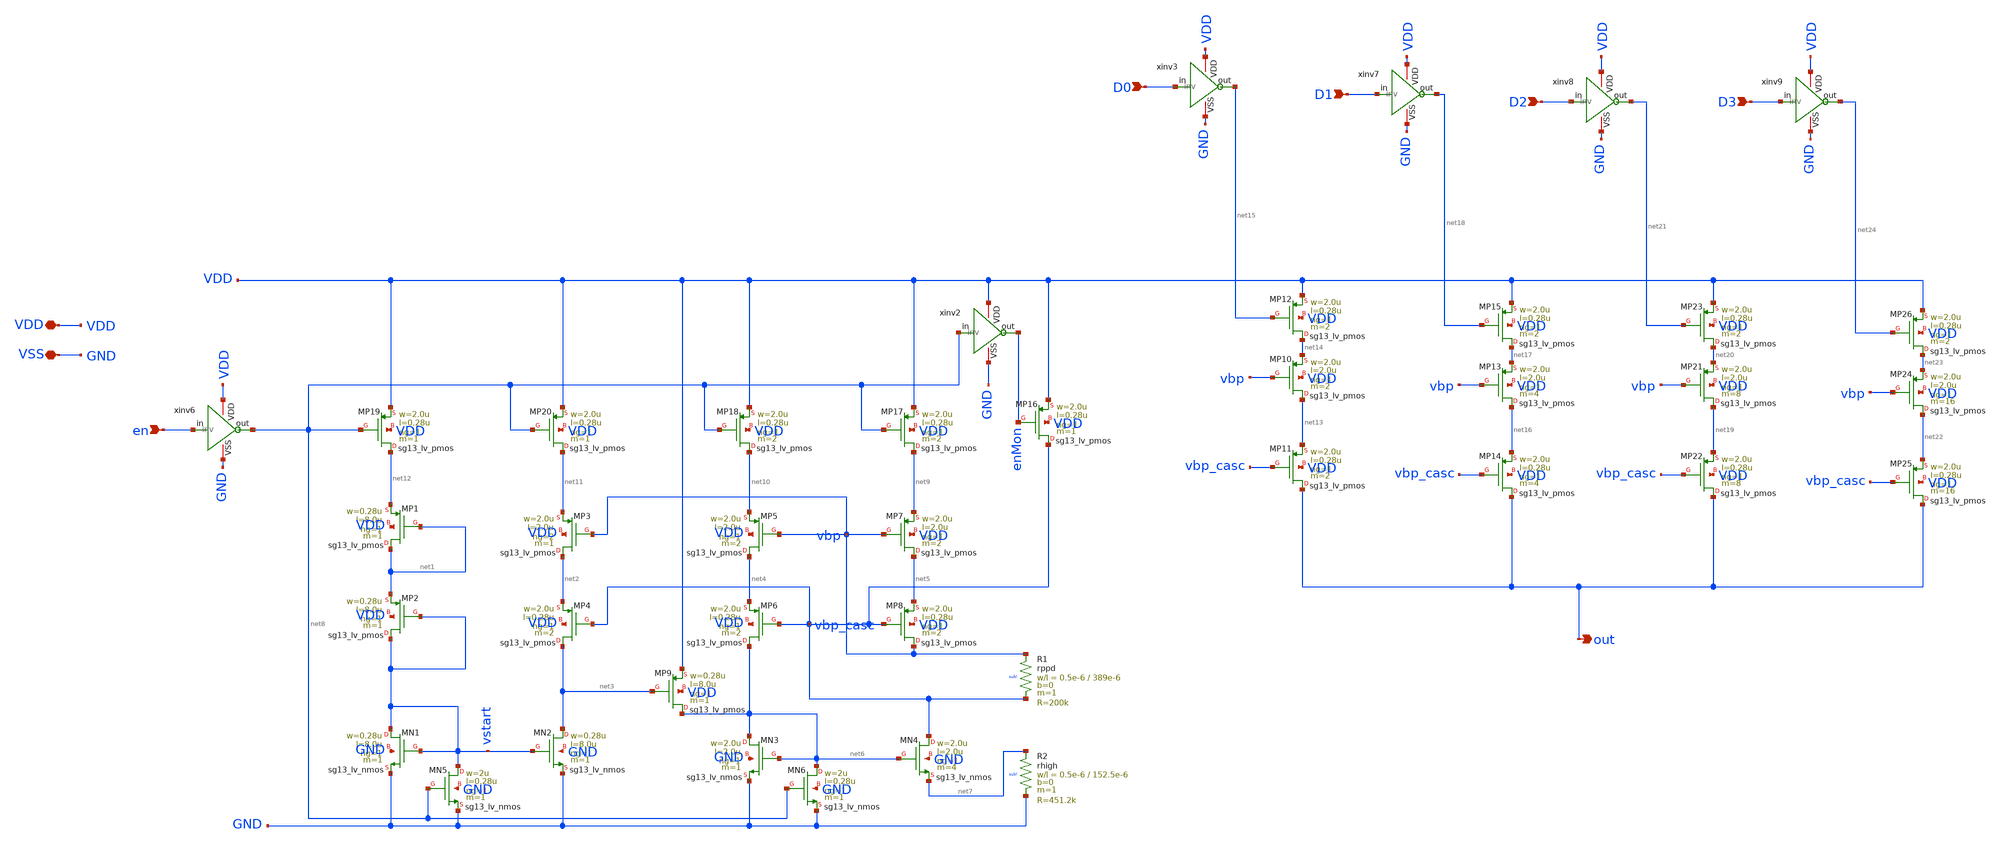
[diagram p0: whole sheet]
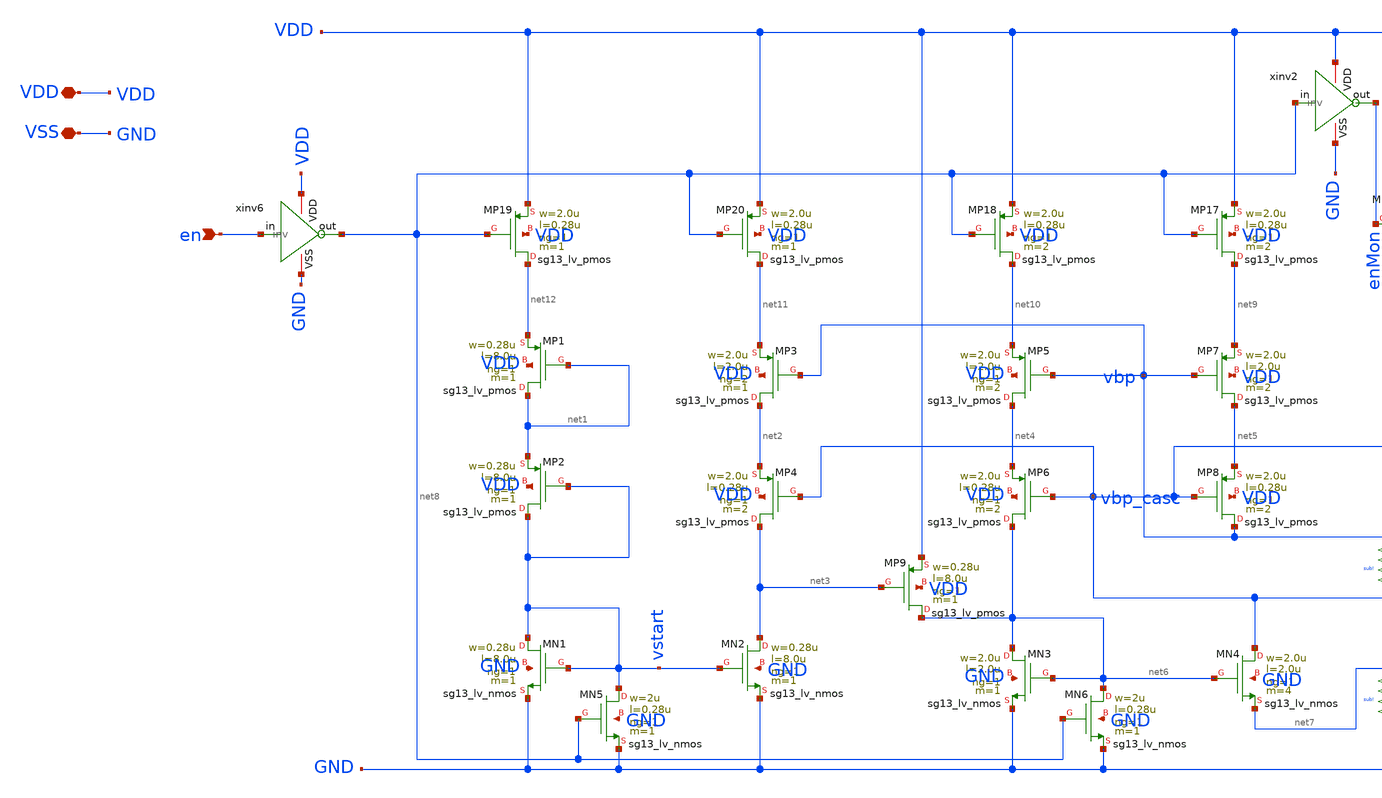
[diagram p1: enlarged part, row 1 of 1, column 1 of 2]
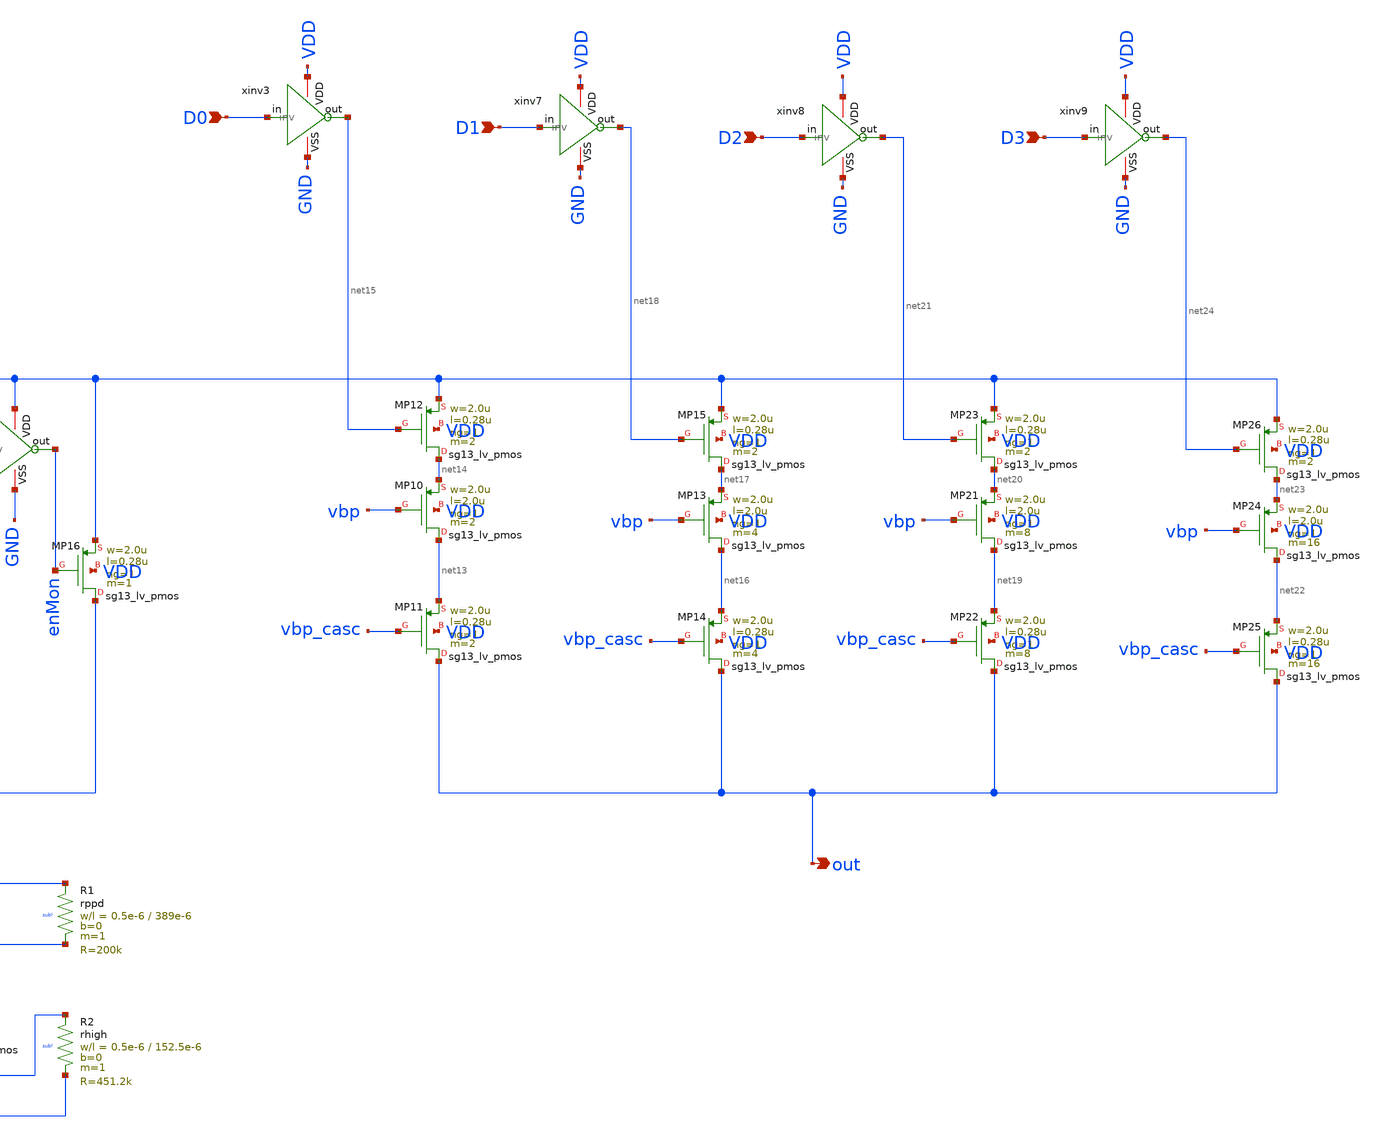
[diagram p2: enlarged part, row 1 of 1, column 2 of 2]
** sch_path: blocks/composite/dpi_adexp_neuron/design_data/xschem/trimmer.sch
**.subckt trimmer en D0 D1 D2 D3 out VDD VSS
*.ipin en
*.ipin D0
*.ipin D1
*.ipin D2
*.ipin D3
*.opin out
*.iopin VDD
*.iopin VSS
XMP1 net1 net1 net12 VDD sg13_lv_pmos w=0.28u l=8.0u ng=1 m=1 mm_ok=1
XMP2 vstart vstart net1 VDD sg13_lv_pmos w=0.28u l=8.0u ng=1 m=1 mm_ok=1
XMN2 net3 vstart GND GND sg13_lv_nmos w=0.28u l=8.0u ng=1 m=1 mm_ok=1
XMN1 vstart vstart GND GND sg13_lv_nmos w=0.28u l=8.0u ng=1 m=1 mm_ok=1
XMP3 net2 vbp net11 VDD sg13_lv_pmos w=2.0u l=2.0u ng=2 m=1 mm_ok=1
XMP4 net3 vbp_casc net2 VDD sg13_lv_pmos w=2.0u l=0.28u ng=1 m=2 mm_ok=1
XMP5 net4 vbp net10 VDD sg13_lv_pmos w=2.0u l=2.0u ng=1 m=2 mm_ok=1
XMP6 net6 vbp_casc net4 VDD sg13_lv_pmos w=2.0u l=0.28u ng=1 m=2 mm_ok=1
XMP7 net5 vbp net9 VDD sg13_lv_pmos w=2.0u l=2.0u ng=1 m=2 mm_ok=1
XMP8 vbp vbp_casc net5 VDD sg13_lv_pmos w=2.0u l=0.28u ng=1 m=2 mm_ok=1
XMP9 net6 net3 VDD VDD sg13_lv_pmos w=0.28u l=8.0u ng=1 m=1 mm_ok=1
XMN3 net6 net6 GND GND sg13_lv_nmos w=2.0u l=2.0u ng=1 m=1 mm_ok=1
XMN4 vbp_casc net6 net7 GND sg13_lv_nmos w=2.0u l=2.0u ng=1 m=4 mm_ok=1
XR1 vbp vbp_casc sub! rppd w=0.5e-6 l=389e-6 m=1 b=0 mm_ok=1
XR2 net7 GND sub! rhigh w=0.5e-6 l=152.5e-6 m=1 b=0 mm_ok=1
XMP10 net13 vbp net14 VDD sg13_lv_pmos w=2.0u l=2.0u ng=1 m=2 mm_ok=1
XMP11 out vbp_casc net13 VDD sg13_lv_pmos w=2.0u l=0.28u ng=1 m=2 mm_ok=1
XMP16 vbp_casc enMon VDD VDD sg13_lv_pmos w=2.0u l=0.28u ng=1 m=1 mm_ok=1
XMP17 net9 net8 VDD VDD sg13_lv_pmos w=2.0u l=0.28u ng=1 m=2 mm_ok=1
XMP18 net10 net8 VDD VDD sg13_lv_pmos w=2.0u l=0.28u ng=1 m=2 mm_ok=1
XMP19 net12 net8 VDD VDD sg13_lv_pmos w=2.0u l=0.28u ng=1 m=1 mm_ok=1
XMP20 net11 net8 VDD VDD sg13_lv_pmos w=2.0u l=0.28u ng=1 m=1 mm_ok=1
XMN5 vstart net8 GND GND sg13_lv_nmos w=2u l=0.28u ng=1 m=1 mm_ok=1
XMN6 net6 net8 GND GND sg13_lv_nmos w=2u l=0.28u ng=1 m=1 mm_ok=1
xinv2 VDD net8 enMon GND inv
XMP12 net14 net15 VDD VDD sg13_lv_pmos w=2.0u l=0.28u ng=1 m=2 mm_ok=1
XMP13 net16 vbp net17 VDD sg13_lv_pmos w=2.0u l=2.0u ng=1 m=4 mm_ok=1
XMP14 out vbp_casc net16 VDD sg13_lv_pmos w=2.0u l=0.28u ng=1 m=4 mm_ok=1
XMP15 net17 net18 VDD VDD sg13_lv_pmos w=2.0u l=0.28u ng=1 m=2 mm_ok=1
XMP21 net19 vbp net20 VDD sg13_lv_pmos w=2.0u l=2.0u ng=1 m=8 mm_ok=1
XMP22 out vbp_casc net19 VDD sg13_lv_pmos w=2.0u l=0.28u ng=1 m=8 mm_ok=1
XMP23 net20 net21 VDD VDD sg13_lv_pmos w=2.0u l=0.28u ng=1 m=2 mm_ok=1
XMP24 net22 vbp net23 VDD sg13_lv_pmos w=2.0u l=2.0u ng=1 m=16 mm_ok=1
XMP25 out vbp_casc net22 VDD sg13_lv_pmos w=2.0u l=0.28u ng=1 m=16 mm_ok=1
XMP26 net23 net24 VDD VDD sg13_lv_pmos w=2.0u l=0.28u ng=1 m=2 mm_ok=1
xinv6 VDD en net8 GND inv
xinv3 VDD D0 net15 GND inv
xinv7 VDD D1 net18 GND inv
xinv8 VDD D2 net21 GND inv
xinv9 VDD D3 net24 GND inv
**.ends

* expanding   symbol:  inv.sym # of pins=4
** sym_path: blocks/composite/dpi_adexp_neuron/design_data/xschem/dev/inv.sym
** sch_path: blocks/composite/dpi_adexp_neuron/design_data/xschem/dev/inv.sch
.subckt inv VDD in out VSS
*.iopin VDD
*.ipin in
*.iopin VSS
*.opin out
XM1 out in VSS VSS sg13_lv_nmos w=2.0u l=0.28u ng=1 m=1 mm_ok=1
XM2 out in VDD VDD sg13_lv_pmos w=2.0u l=0.28u ng=1 m=1 mm_ok=1
.ends

.end
